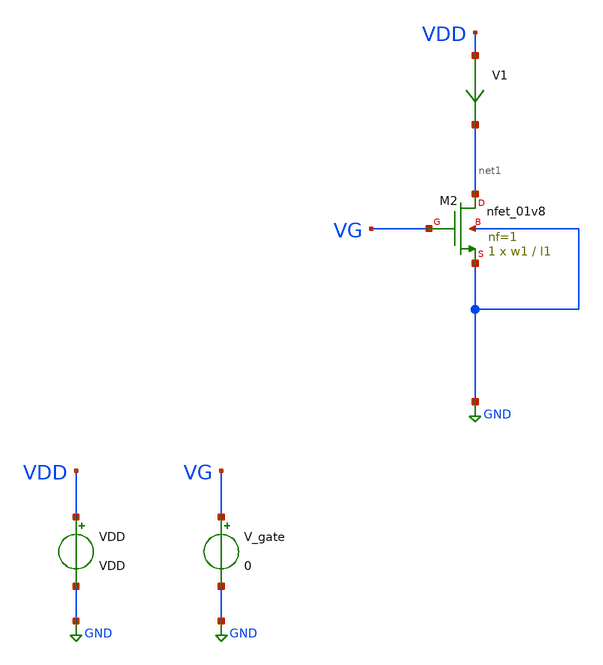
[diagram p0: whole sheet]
** sch_path: TESTS/transistor_tests/nfet_01v8_test.sch
**.subckt nfet_01v8_test
XM2 net1 VG GND GND sky130_fd_pr__nfet_01v8 L=l1 W=w1 nf=1 ad='int((1 + 1)/2) * w1 / 1 * 0.29' as='int((1 + 2)/2) * w1 / 1 * 0.29'
+ pd='2*int((1 + 1)/2) * (w1 / 1 + 0.29)' ps='2*int((1 + 2)/2) * (w1 / 1 + 0.29)' nrd='0.29 / w1 ' nrs='0.29 / w1 '
+ sa=0 sb=0 sd=0 mult=1 m=1
VDD VDD GND VDD
V_gate VG GND 0
V1 VDD net1 0
.save i(v1)
**** begin user architecture code

** opencircuitdesign pdks install
.lib $::SKYWATER_MODELS/sky130.lib.spice tt

.param VDD = 1.8
.param w1 = 1
.param l1 = 1.5
.TEMP 100


.control
  save all
  dc V_gate 0 1.8 0.0001
  plot i(V1)
  wrdata /home/vasco/Desktop/sky130A/TESTS/transistor_tests/nfet_01v8_dc_vgs.txt i(V1)


.endc


**** end user architecture code
**.ends
.GLOBAL GND
.end
